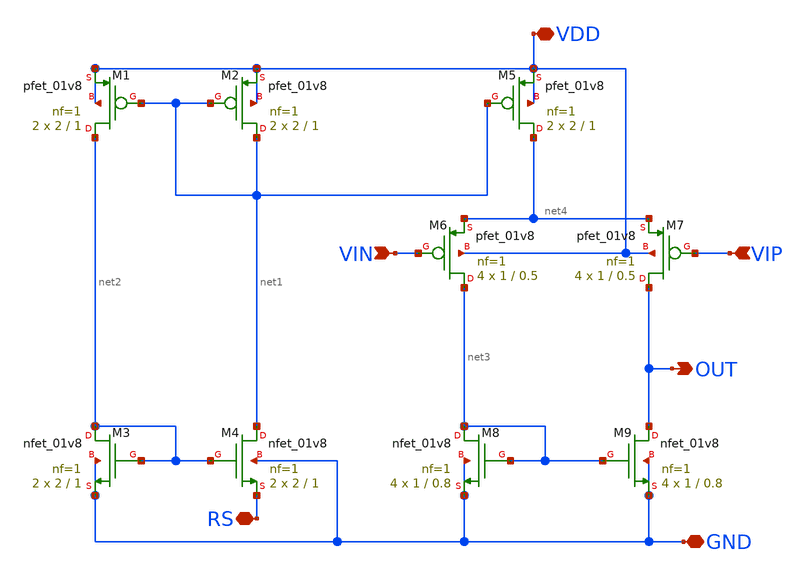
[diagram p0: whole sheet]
** sch_path: Op-Amp/xschem/Op-Amp.sch
**.subckt Op-Amp VIN VIP GND VDD RS OUT
*.ipin VIN
*.ipin VIP
*.iopin GND
*.iopin VDD
*.iopin RS
*.opin OUT
XM1 net2 net1 VDD VDD sky130_fd_pr__pfet_01v8 L=1 W=2 nf=1 ad='int((nf+1)/2) * W/nf * 0.29' as='int((nf+2)/2) * W/nf * 0.29'
+ pd='2*int((nf+1)/2) * (W/nf + 0.29)' ps='2*int((nf+2)/2) * (W/nf + 0.29)' nrd='0.29 / W' nrs='0.29 / W'
+ sa=0 sb=0 sd=0 mult=2 m=2
XM2 net1 net1 VDD VDD sky130_fd_pr__pfet_01v8 L=1 W=2 nf=1 ad='int((nf+1)/2) * W/nf * 0.29' as='int((nf+2)/2) * W/nf * 0.29'
+ pd='2*int((nf+1)/2) * (W/nf + 0.29)' ps='2*int((nf+2)/2) * (W/nf + 0.29)' nrd='0.29 / W' nrs='0.29 / W'
+ sa=0 sb=0 sd=0 mult=2 m=2
XM3 net2 net2 GND GND sky130_fd_pr__nfet_01v8 L=1 W=2 nf=1 ad='int((nf+1)/2) * W/nf * 0.29' as='int((nf+2)/2) * W/nf * 0.29'
+ pd='2*int((nf+1)/2) * (W/nf + 0.29)' ps='2*int((nf+2)/2) * (W/nf + 0.29)' nrd='0.29 / W' nrs='0.29 / W'
+ sa=0 sb=0 sd=0 mult=2 m=2
XM4 net1 net2 RS GND sky130_fd_pr__nfet_01v8 L=1 W=2 nf=1 ad='int((nf+1)/2) * W/nf * 0.29' as='int((nf+2)/2) * W/nf * 0.29'
+ pd='2*int((nf+1)/2) * (W/nf + 0.29)' ps='2*int((nf+2)/2) * (W/nf + 0.29)' nrd='0.29 / W' nrs='0.29 / W'
+ sa=0 sb=0 sd=0 mult=2 m=2
XM5 net4 net1 VDD VDD sky130_fd_pr__pfet_01v8 L=1 W=2 nf=1 ad='int((nf+1)/2) * W/nf * 0.29' as='int((nf+2)/2) * W/nf * 0.29'
+ pd='2*int((nf+1)/2) * (W/nf + 0.29)' ps='2*int((nf+2)/2) * (W/nf + 0.29)' nrd='0.29 / W' nrs='0.29 / W'
+ sa=0 sb=0 sd=0 mult=2 m=2
XM6 net3 VIN net4 VDD sky130_fd_pr__pfet_01v8 L=0.5 W=1 nf=1 ad='int((nf+1)/2) * W/nf * 0.29' as='int((nf+2)/2) * W/nf * 0.29'
+ pd='2*int((nf+1)/2) * (W/nf + 0.29)' ps='2*int((nf+2)/2) * (W/nf + 0.29)' nrd='0.29 / W' nrs='0.29 / W'
+ sa=0 sb=0 sd=0 mult=4 m=4
XM7 OUT VIP net4 VDD sky130_fd_pr__pfet_01v8 L=0.5 W=1 nf=1 ad='int((nf+1)/2) * W/nf * 0.29' as='int((nf+2)/2) * W/nf * 0.29'
+ pd='2*int((nf+1)/2) * (W/nf + 0.29)' ps='2*int((nf+2)/2) * (W/nf + 0.29)' nrd='0.29 / W' nrs='0.29 / W'
+ sa=0 sb=0 sd=0 mult=4 m=4
XM8 net3 net3 GND GND sky130_fd_pr__nfet_01v8 L=0.8 W=1 nf=1 ad='int((nf+1)/2) * W/nf * 0.29' as='int((nf+2)/2) * W/nf * 0.29'
+ pd='2*int((nf+1)/2) * (W/nf + 0.29)' ps='2*int((nf+2)/2) * (W/nf + 0.29)' nrd='0.29 / W' nrs='0.29 / W'
+ sa=0 sb=0 sd=0 mult=4 m=4
XM9 OUT net3 GND GND sky130_fd_pr__nfet_01v8 L=0.8 W=1 nf=1 ad='int((nf+1)/2) * W/nf * 0.29' as='int((nf+2)/2) * W/nf * 0.29'
+ pd='2*int((nf+1)/2) * (W/nf + 0.29)' ps='2*int((nf+2)/2) * (W/nf + 0.29)' nrd='0.29 / W' nrs='0.29 / W'
+ sa=0 sb=0 sd=0 mult=4 m=4
**.ends
.end
